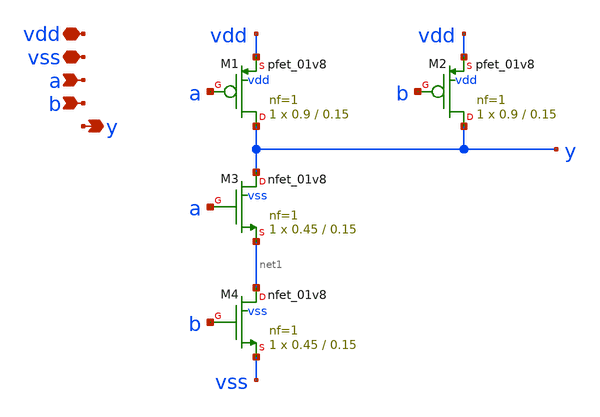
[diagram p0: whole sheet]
** sch_path: xschem/sc_nand2.sch
**.subckt sc_nand2 vdd vss a y b
*.iopin vdd
*.iopin vss
*.ipin a
*.opin y
*.ipin b
XM1 y a vdd vdd sky130_fd_pr__pfet_01v8 L=0.15 W=0.9 nf=1 ad='int((1 + 1)/2) * 0.9 / 1 * 0.29' as='int((1 + 2)/2) * 0.9 / 1 * 0.29'
+ pd='2*int((1 + 1)/2) * (0.9 / 1 + 0.29)' ps='2*int((1 + 2)/2) * (0.9 / 1 + 0.29)' nrd='0.29 / 0.9 ' nrs='0.29 / 0.9 '
+ sa=0 sb=0 sd=0 mult=1 m=1
XM2 y b vdd vdd sky130_fd_pr__pfet_01v8 L=0.15 W=0.9 nf=1 ad='int((1 + 1)/2) * 0.9 / 1 * 0.29' as='int((1 + 2)/2) * 0.9 / 1 * 0.29'
+ pd='2*int((1 + 1)/2) * (0.9 / 1 + 0.29)' ps='2*int((1 + 2)/2) * (0.9 / 1 + 0.29)' nrd='0.29 / 0.9 ' nrs='0.29 / 0.9 '
+ sa=0 sb=0 sd=0 mult=1 m=1
XM3 y a net1 vss sky130_fd_pr__nfet_01v8 L=0.15 W=0.45 nf=1 ad='int((nf+1)/2) * W/nf * 0.29' as='int((nf+2)/2) * W/nf * 0.29'
+ pd='2*int((nf+1)/2) * (W/nf + 0.29)' ps='2*int((nf+2)/2) * (W/nf + 0.29)' nrd='0.29 / W' nrs='0.29 / W'
+ sa=0 sb=0 sd=0 mult=1 m=1
XM4 net1 b vss vss sky130_fd_pr__nfet_01v8 L=0.15 W=0.45 nf=1 ad='int((nf+1)/2) * W/nf * 0.29' as='int((nf+2)/2) * W/nf * 0.29'
+ pd='2*int((nf+1)/2) * (W/nf + 0.29)' ps='2*int((nf+2)/2) * (W/nf + 0.29)' nrd='0.29 / W' nrs='0.29 / W'
+ sa=0 sb=0 sd=0 mult=1 m=1
**.ends
.end
